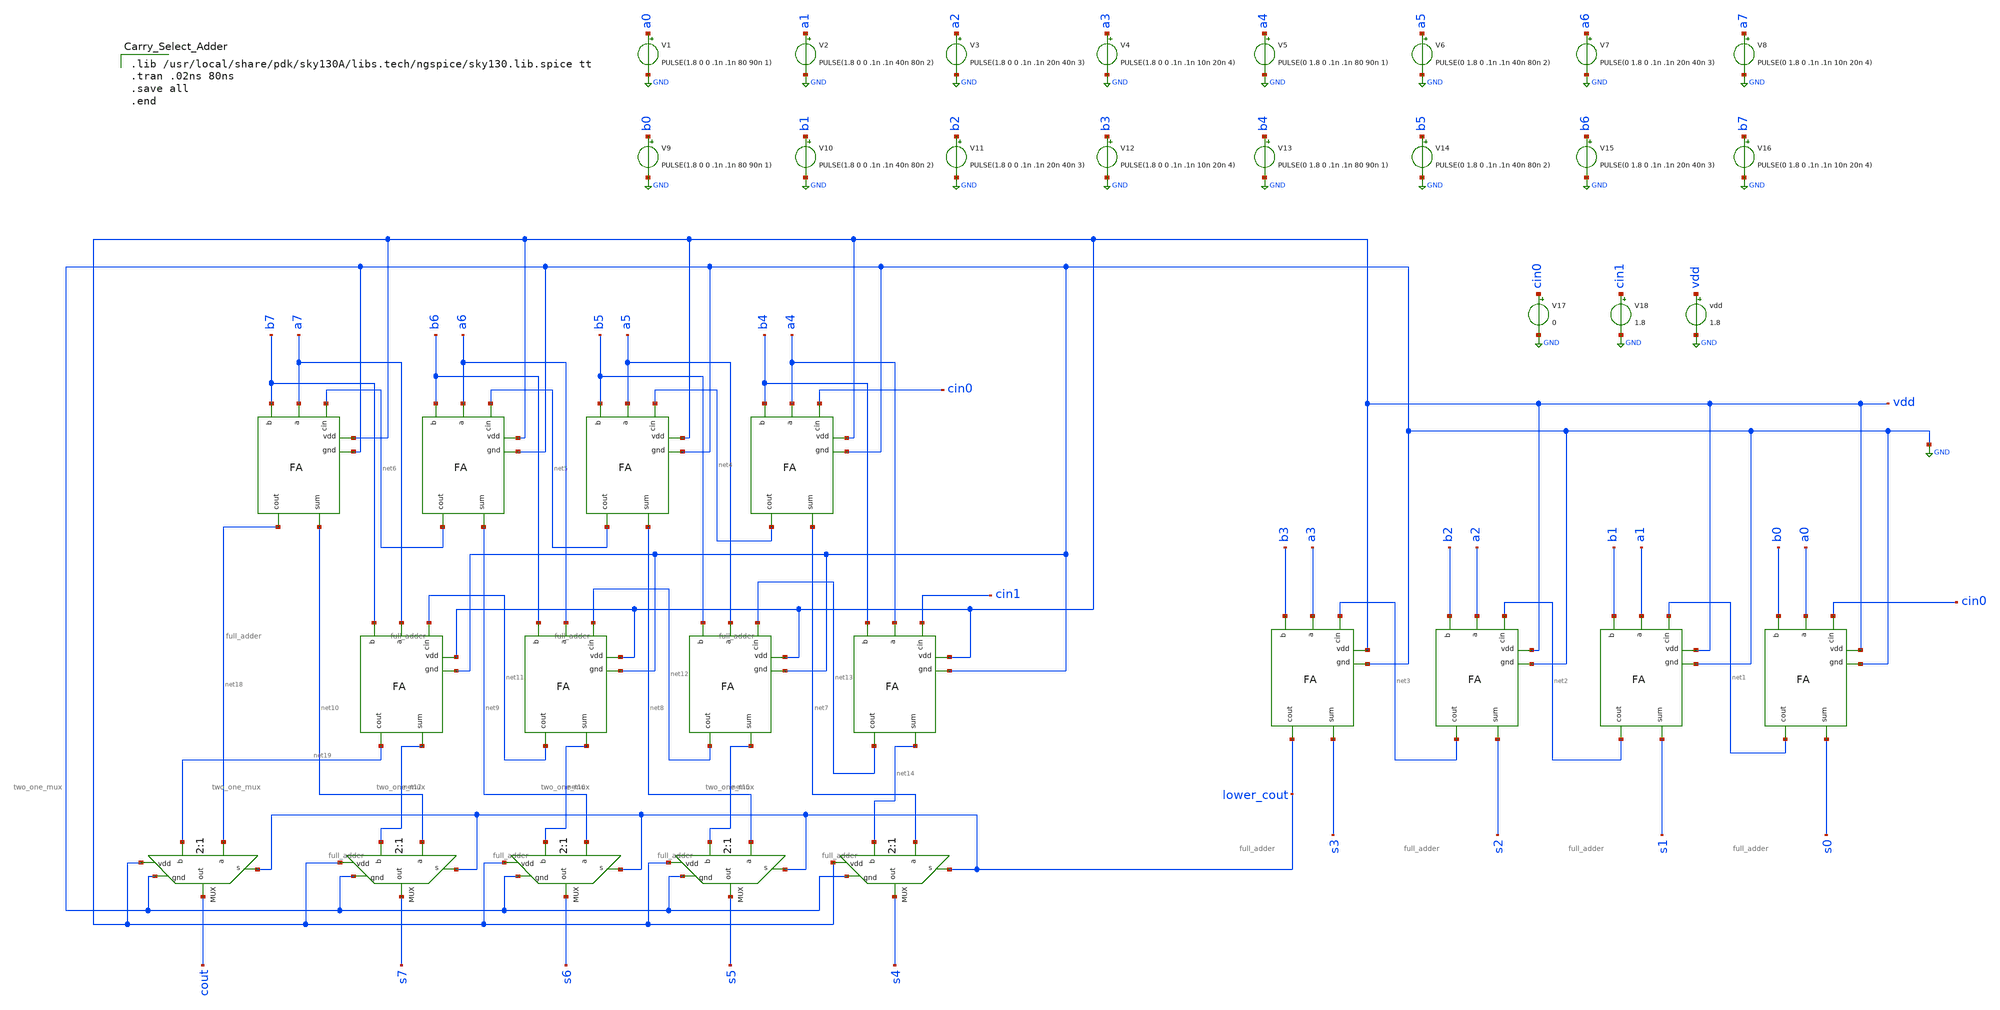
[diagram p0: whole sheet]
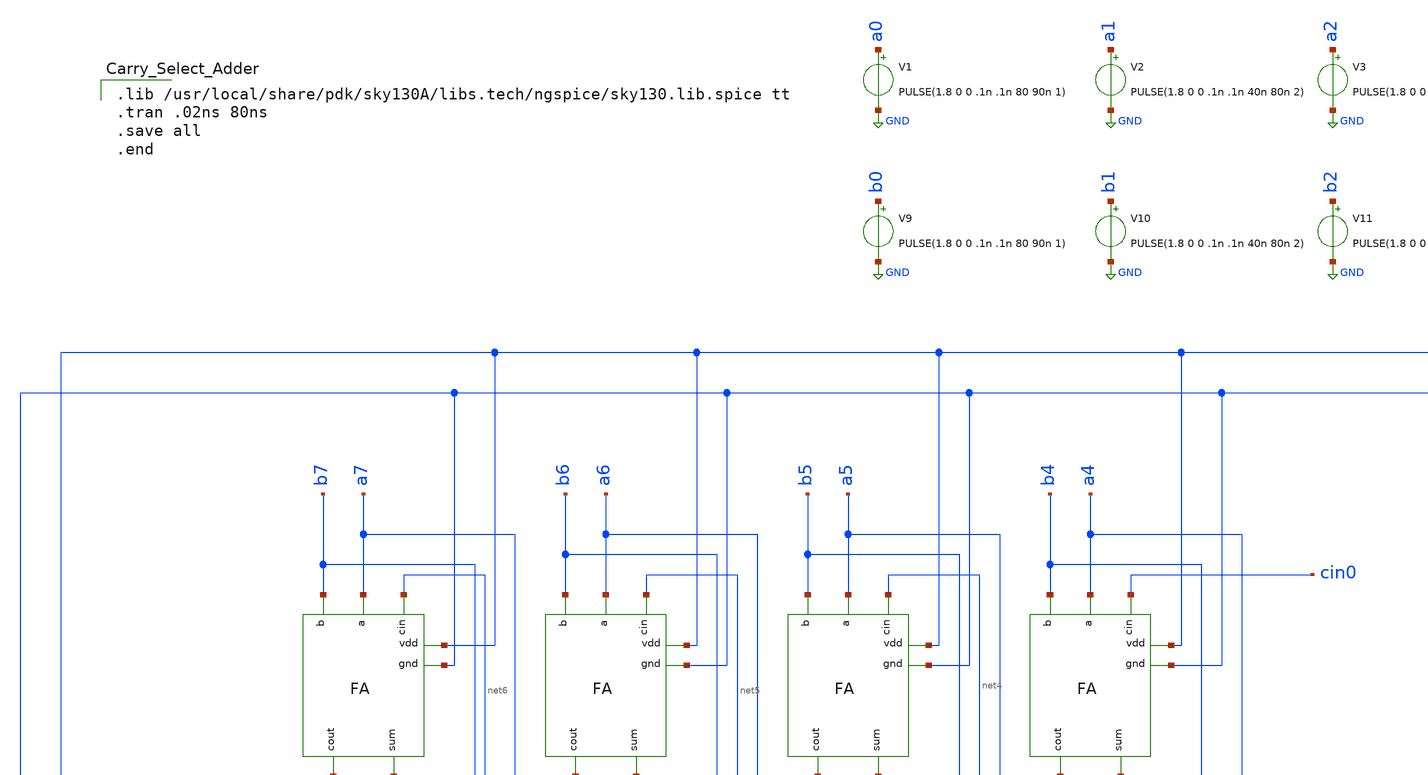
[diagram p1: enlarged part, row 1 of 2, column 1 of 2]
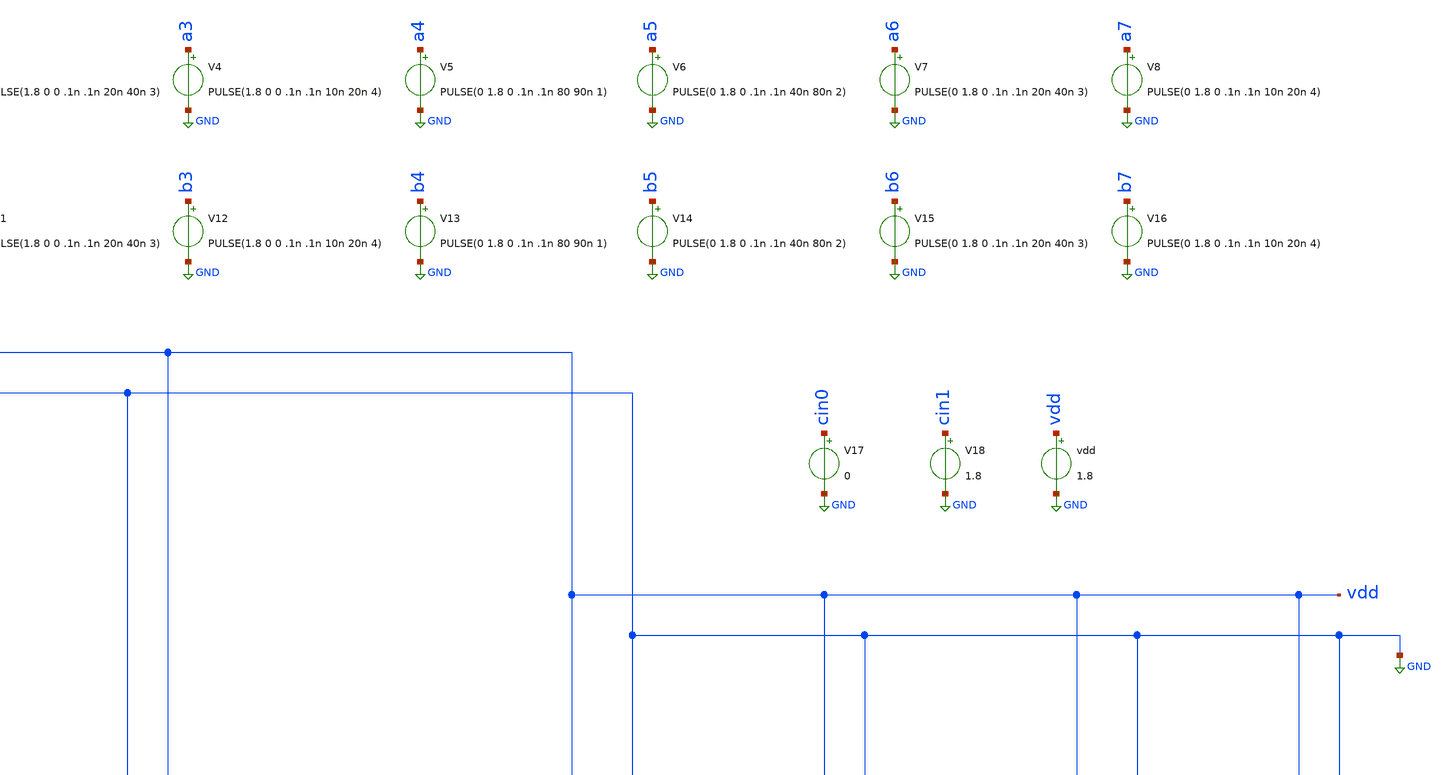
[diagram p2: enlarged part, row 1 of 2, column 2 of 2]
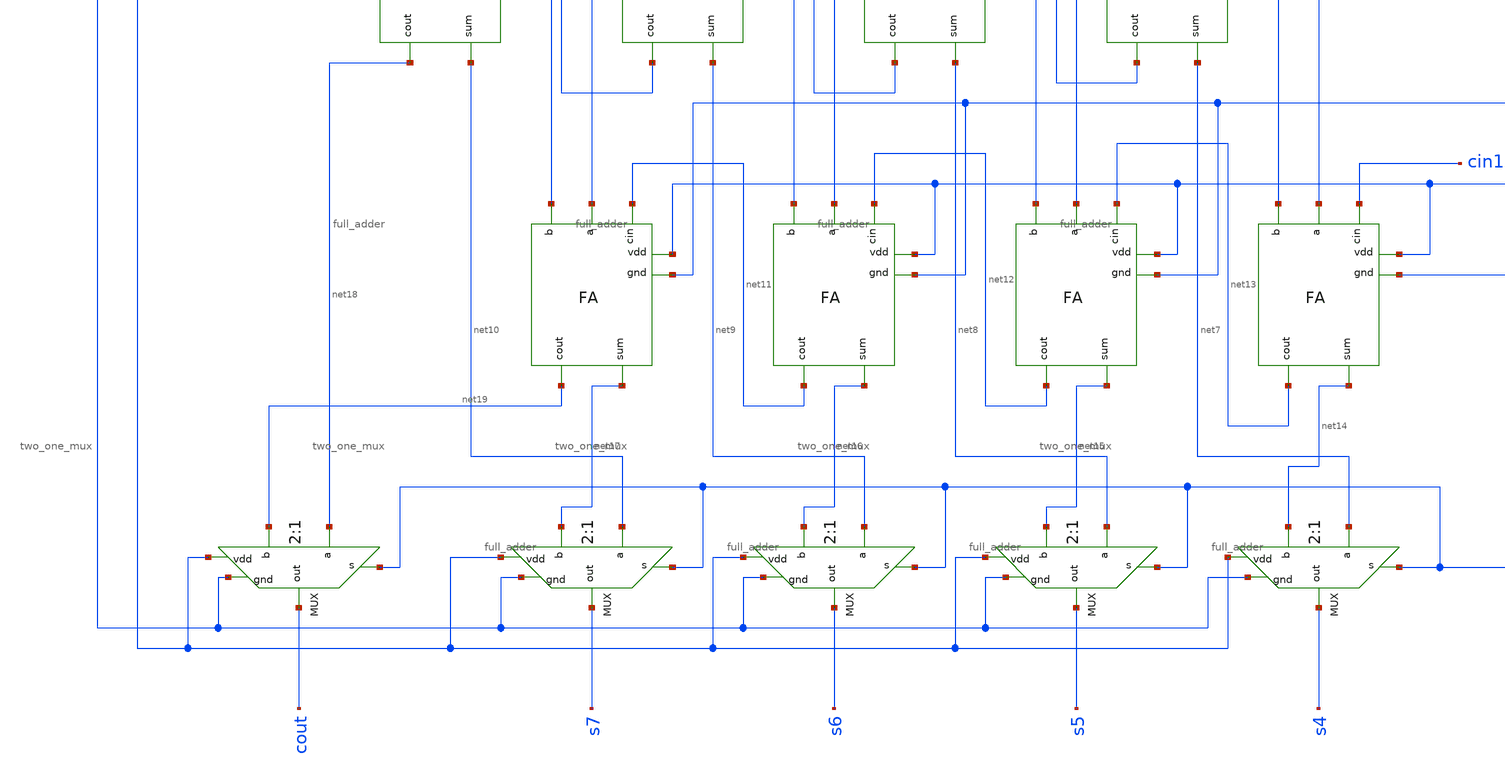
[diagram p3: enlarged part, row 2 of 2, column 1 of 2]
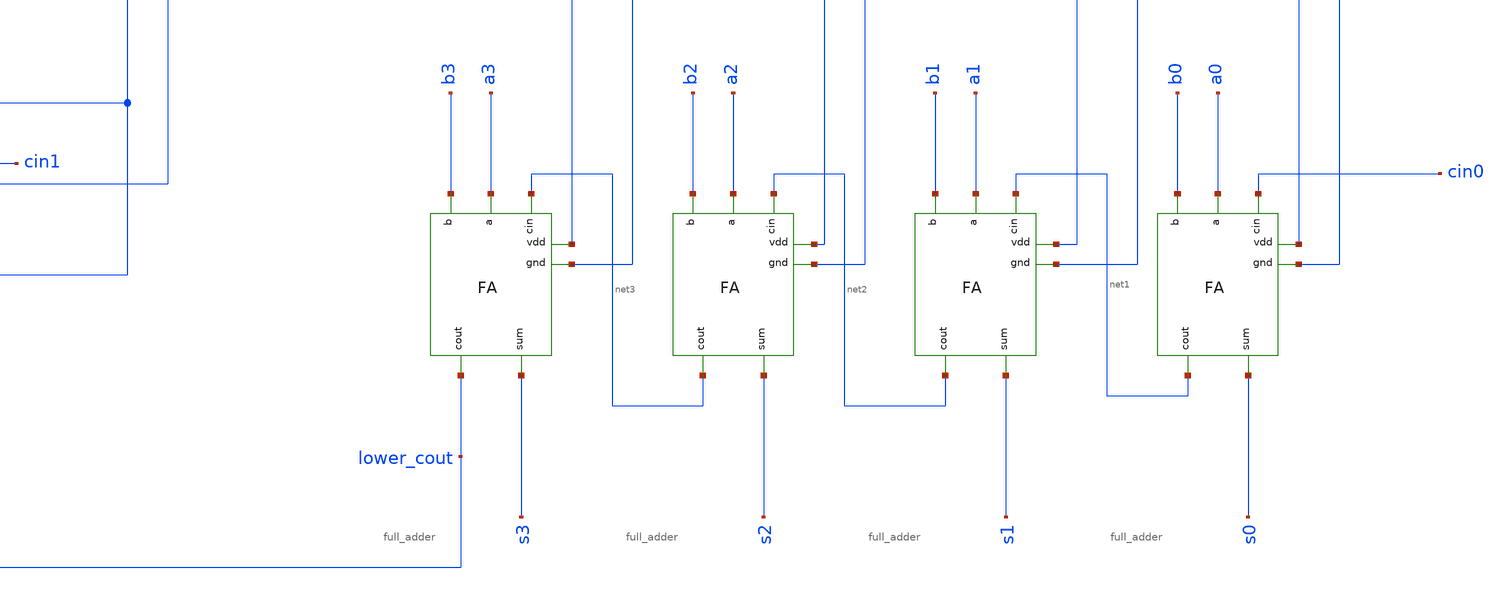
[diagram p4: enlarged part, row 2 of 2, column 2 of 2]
** sch_path: Projects/Design_and_Analysis_of_8-bit_Carry_Select_Adder_Schematic_Design_Layout_Design_and_LVS_Validation_using_SKY130PDK/assets/files/schematic/carry_select_adder.sch
**.subckt carry_select_adder
x1 s3 lower_cout vdd GND net3 a3 b3 full_adder
x2 s2 net3 vdd GND net2 a2 b2 full_adder
x3 s1 net2 vdd GND net1 a1 b1 full_adder
x4 s0 net1 vdd GND cin0 a0 b0 full_adder
x5 net10 net18 vdd GND net6 a7 b7 full_adder
x6 net9 net6 vdd GND net5 a6 b6 full_adder
x7 net8 net5 vdd GND net4 a5 b5 full_adder
x8 net7 net4 vdd GND cin0 a4 b4 full_adder
x9 net17 net19 vdd GND net11 a7 b7 full_adder
x10 net16 net11 vdd GND net12 a6 b6 full_adder
x11 net15 net12 vdd GND net13 a5 b5 full_adder
x12 net14 net13 vdd GND cin1 a4 b4 full_adder
x13 s7 lower_cout net10 net17 vdd GND two_one_mux
x14 s6 lower_cout net9 net16 vdd GND two_one_mux
x15 s5 lower_cout net8 net15 vdd GND two_one_mux
x16 s4 lower_cout net7 net14 vdd GND two_one_mux
x17 cout lower_cout net18 net19 vdd GND two_one_mux
V17 cin0 GND 0
V18 cin1 GND 1.8
vdd vdd GND 1.8
V1 a0 GND PULSE(1.8 0 0 .1n .1n 80 90n 1)
V2 a1 GND PULSE(1.8 0 0 .1n .1n 40n 80n 2)
V3 a2 GND PULSE(1.8 0 0 .1n .1n 20n 40n 3)
V4 a3 GND PULSE(1.8 0 0 .1n .1n 10n 20n 4)
V5 a4 GND PULSE(0 1.8 0 .1n .1n 80 90n 1)
V6 a5 GND PULSE(0 1.8 0 .1n .1n 40n 80n 2)
V7 a6 GND PULSE(0 1.8 0 .1n .1n 20n 40n 3)
V8 a7 GND PULSE(0 1.8 0 .1n .1n 10n 20n 4)
V9 b0 GND PULSE(1.8 0 0 .1n .1n 80 90n 1)
V10 b1 GND PULSE(1.8 0 0 .1n .1n 40n 80n 2)
V11 b2 GND PULSE(1.8 0 0 .1n .1n 20n 40n 3)
V12 b3 GND PULSE(1.8 0 0 .1n .1n 10n 20n 4)
V13 b4 GND PULSE(0 1.8 0 .1n .1n 80 90n 1)
V14 b5 GND PULSE(0 1.8 0 .1n .1n 40n 80n 2)
V15 b6 GND PULSE(0 1.8 0 .1n .1n 20n 40n 3)
V16 b7 GND PULSE(0 1.8 0 .1n .1n 10n 20n 4)
**** begin user architecture code

.lib /usr/local/share/pdk/sky130A/libs.tech/ngspice/sky130.lib.spice tt
.tran .02ns 80ns
.save all
.end

**** end user architecture code
**.ends

* expanding   symbol:  full_adder.sym # of pins=7
** sym_path: Projects/Design_and_Analysis_of_8-bit_Carry_Select_Adder_Schematic_Design_Layout_Design_and_LVS_Validation_using_SKY130PDK/assets/files/schematic/full_adder.sym
** sch_path: Projects/Design_and_Analysis_of_8-bit_Carry_Select_Adder_Schematic_Design_Layout_Design_and_LVS_Validation_using_SKY130PDK/assets/files/schematic/full_adder.sch
.subckt full_adder sum cout vdd gnd cin a b
*.ipin a
*.ipin b
*.ipin cin
*.opin cout
*.opin sum
*.ipin vdd
*.ipin gnd
XM27 sum net1 vdd vdd sky130_fd_pr__pfet_01v8 L=0.15 W=2 nf=1 ad='int((nf+1)/2) * W/nf * 0.29' as='int((nf+2)/2) * W/nf * 0.29'
+ pd='2*int((nf+1)/2) * (W/nf + 0.29)' ps='2*int((nf+2)/2) * (W/nf + 0.29)' nrd='0.29 / W' nrs='0.29 / W'
+ sa=0 sb=0 sd=0 mult=1 m=1
XM28 sum net1 gnd gnd sky130_fd_pr__nfet_01v8 L=0.15 W=1 nf=1 ad='int((nf+1)/2) * W/nf * 0.29' as='int((nf+2)/2) * W/nf * 0.29'
+ pd='2*int((nf+1)/2) * (W/nf + 0.29)' ps='2*int((nf+2)/2) * (W/nf + 0.29)' nrd='0.29 / W' nrs='0.29 / W'
+ sa=0 sb=0 sd=0 mult=1 m=1
XM11 cout net2 vdd vdd sky130_fd_pr__pfet_01v8 L=0.15 W=2 nf=1 ad='int((nf+1)/2) * W/nf * 0.29' as='int((nf+2)/2) * W/nf * 0.29'
+ pd='2*int((nf+1)/2) * (W/nf + 0.29)' ps='2*int((nf+2)/2) * (W/nf + 0.29)' nrd='0.29 / W' nrs='0.29 / W'
+ sa=0 sb=0 sd=0 mult=1 m=1
XM12 cout net2 gnd gnd sky130_fd_pr__nfet_01v8 L=0.15 W=1 nf=1 ad='int((nf+1)/2) * W/nf * 0.29' as='int((nf+2)/2) * W/nf * 0.29'
+ pd='2*int((nf+1)/2) * (W/nf + 0.29)' ps='2*int((nf+2)/2) * (W/nf + 0.29)' nrd='0.29 / W' nrs='0.29 / W'
+ sa=0 sb=0 sd=0 mult=1 m=1
XM1 net2 cin net4 gnd sky130_fd_pr__nfet_01v8 L=0.15 W=2 nf=1 ad='int((nf+1)/2) * W/nf * 0.29' as='int((nf+2)/2) * W/nf * 0.29'
+ pd='2*int((nf+1)/2) * (W/nf + 0.29)' ps='2*int((nf+2)/2) * (W/nf + 0.29)' nrd='0.29 / W' nrs='0.29 / W'
+ sa=0 sb=0 sd=0 mult=1 m=1
XM2 net3 a vdd vdd sky130_fd_pr__pfet_01v8 L=0.15 W=4 nf=1 ad='int((nf+1)/2) * W/nf * 0.29' as='int((nf+2)/2) * W/nf * 0.29'
+ pd='2*int((nf+1)/2) * (W/nf + 0.29)' ps='2*int((nf+2)/2) * (W/nf + 0.29)' nrd='0.29 / W' nrs='0.29 / W'
+ sa=0 sb=0 sd=0 mult=1 m=1
XM3 net3 b vdd vdd sky130_fd_pr__pfet_01v8 L=0.15 W=4 nf=1 ad='int((nf+1)/2) * W/nf * 0.29' as='int((nf+2)/2) * W/nf * 0.29'
+ pd='2*int((nf+1)/2) * (W/nf + 0.29)' ps='2*int((nf+2)/2) * (W/nf + 0.29)' nrd='0.29 / W' nrs='0.29 / W'
+ sa=0 sb=0 sd=0 mult=1 m=1
XM4 net2 cin net3 vdd sky130_fd_pr__pfet_01v8 L=0.15 W=4 nf=1 ad='int((nf+1)/2) * W/nf * 0.29' as='int((nf+2)/2) * W/nf * 0.29'
+ pd='2*int((nf+1)/2) * (W/nf + 0.29)' ps='2*int((nf+2)/2) * (W/nf + 0.29)' nrd='0.29 / W' nrs='0.29 / W'
+ sa=0 sb=0 sd=0 mult=1 m=1
XM5 net4 a gnd gnd sky130_fd_pr__nfet_01v8 L=0.15 W=2 nf=1 ad='int((nf+1)/2) * W/nf * 0.29' as='int((nf+2)/2) * W/nf * 0.29'
+ pd='2*int((nf+1)/2) * (W/nf + 0.29)' ps='2*int((nf+2)/2) * (W/nf + 0.29)' nrd='0.29 / W' nrs='0.29 / W'
+ sa=0 sb=0 sd=0 mult=1 m=1
XM6 net4 b gnd gnd sky130_fd_pr__nfet_01v8 L=0.15 W=2 nf=1 ad='int((nf+1)/2) * W/nf * 0.29' as='int((nf+2)/2) * W/nf * 0.29'
+ pd='2*int((nf+1)/2) * (W/nf + 0.29)' ps='2*int((nf+2)/2) * (W/nf + 0.29)' nrd='0.29 / W' nrs='0.29 / W'
+ sa=0 sb=0 sd=0 mult=1 m=1
XM7 net2 a net6 vdd sky130_fd_pr__pfet_01v8 L=0.15 W=4 nf=1 ad='int((nf+1)/2) * W/nf * 0.29' as='int((nf+2)/2) * W/nf * 0.29'
+ pd='2*int((nf+1)/2) * (W/nf + 0.29)' ps='2*int((nf+2)/2) * (W/nf + 0.29)' nrd='0.29 / W' nrs='0.29 / W'
+ sa=0 sb=0 sd=0 mult=1 m=1
XM8 net6 b vdd vdd sky130_fd_pr__pfet_01v8 L=0.15 W=4 nf=1 ad='int((nf+1)/2) * W/nf * 0.29' as='int((nf+2)/2) * W/nf * 0.29'
+ pd='2*int((nf+1)/2) * (W/nf + 0.29)' ps='2*int((nf+2)/2) * (W/nf + 0.29)' nrd='0.29 / W' nrs='0.29 / W'
+ sa=0 sb=0 sd=0 mult=1 m=1
XM9 net2 a net5 gnd sky130_fd_pr__nfet_01v8 L=0.15 W=2 nf=1 ad='int((nf+1)/2) * W/nf * 0.29' as='int((nf+2)/2) * W/nf * 0.29'
+ pd='2*int((nf+1)/2) * (W/nf + 0.29)' ps='2*int((nf+2)/2) * (W/nf + 0.29)' nrd='0.29 / W' nrs='0.29 / W'
+ sa=0 sb=0 sd=0 mult=1 m=1
XM10 net5 b gnd gnd sky130_fd_pr__nfet_01v8 L=0.15 W=2 nf=1 ad='int((nf+1)/2) * W/nf * 0.29' as='int((nf+2)/2) * W/nf * 0.29'
+ pd='2*int((nf+1)/2) * (W/nf + 0.29)' ps='2*int((nf+2)/2) * (W/nf + 0.29)' nrd='0.29 / W' nrs='0.29 / W'
+ sa=0 sb=0 sd=0 mult=1 m=1
XM13 net8 a vdd vdd sky130_fd_pr__pfet_01v8 L=0.15 W=4 nf=1 ad='int((nf+1)/2) * W/nf * 0.29' as='int((nf+2)/2) * W/nf * 0.29'
+ pd='2*int((nf+1)/2) * (W/nf + 0.29)' ps='2*int((nf+2)/2) * (W/nf + 0.29)' nrd='0.29 / W' nrs='0.29 / W'
+ sa=0 sb=0 sd=0 mult=1 m=1
XM14 net8 b vdd vdd sky130_fd_pr__pfet_01v8 L=0.15 W=4 nf=1 ad='int((nf+1)/2) * W/nf * 0.29' as='int((nf+2)/2) * W/nf * 0.29'
+ pd='2*int((nf+1)/2) * (W/nf + 0.29)' ps='2*int((nf+2)/2) * (W/nf + 0.29)' nrd='0.29 / W' nrs='0.29 / W'
+ sa=0 sb=0 sd=0 mult=1 m=1
XM15 net8 cin vdd vdd sky130_fd_pr__pfet_01v8 L=0.15 W=4 nf=1 ad='int((nf+1)/2) * W/nf * 0.29' as='int((nf+2)/2) * W/nf * 0.29'
+ pd='2*int((nf+1)/2) * (W/nf + 0.29)' ps='2*int((nf+2)/2) * (W/nf + 0.29)' nrd='0.29 / W' nrs='0.29 / W'
+ sa=0 sb=0 sd=0 mult=1 m=1
XM16 net7 a gnd gnd sky130_fd_pr__nfet_01v8 L=0.15 W=2 nf=1 ad='int((nf+1)/2) * W/nf * 0.29' as='int((nf+2)/2) * W/nf * 0.29'
+ pd='2*int((nf+1)/2) * (W/nf + 0.29)' ps='2*int((nf+2)/2) * (W/nf + 0.29)' nrd='0.29 / W' nrs='0.29 / W'
+ sa=0 sb=0 sd=0 mult=1 m=1
XM17 net7 b gnd gnd sky130_fd_pr__nfet_01v8 L=0.15 W=2 nf=1 ad='int((nf+1)/2) * W/nf * 0.29' as='int((nf+2)/2) * W/nf * 0.29'
+ pd='2*int((nf+1)/2) * (W/nf + 0.29)' ps='2*int((nf+2)/2) * (W/nf + 0.29)' nrd='0.29 / W' nrs='0.29 / W'
+ sa=0 sb=0 sd=0 mult=1 m=1
XM18 net7 cin gnd gnd sky130_fd_pr__nfet_01v8 L=0.15 W=2 nf=1 ad='int((nf+1)/2) * W/nf * 0.29' as='int((nf+2)/2) * W/nf * 0.29'
+ pd='2*int((nf+1)/2) * (W/nf + 0.29)' ps='2*int((nf+2)/2) * (W/nf + 0.29)' nrd='0.29 / W' nrs='0.29 / W'
+ sa=0 sb=0 sd=0 mult=1 m=1
XM19 net1 net2 net7 gnd sky130_fd_pr__nfet_01v8 L=0.15 W=2 nf=1 ad='int((nf+1)/2) * W/nf * 0.29' as='int((nf+2)/2) * W/nf * 0.29'
+ pd='2*int((nf+1)/2) * (W/nf + 0.29)' ps='2*int((nf+2)/2) * (W/nf + 0.29)' nrd='0.29 / W' nrs='0.29 / W'
+ sa=0 sb=0 sd=0 mult=1 m=1
XM20 net1 net2 net8 vdd sky130_fd_pr__pfet_01v8 L=0.15 W=4 nf=1 ad='int((nf+1)/2) * W/nf * 0.29' as='int((nf+2)/2) * W/nf * 0.29'
+ pd='2*int((nf+1)/2) * (W/nf + 0.29)' ps='2*int((nf+2)/2) * (W/nf + 0.29)' nrd='0.29 / W' nrs='0.29 / W'
+ sa=0 sb=0 sd=0 mult=1 m=1
XM21 net1 cin net10 vdd sky130_fd_pr__pfet_01v8 L=0.15 W=6 nf=1 ad='int((nf+1)/2) * W/nf * 0.29' as='int((nf+2)/2) * W/nf * 0.29'
+ pd='2*int((nf+1)/2) * (W/nf + 0.29)' ps='2*int((nf+2)/2) * (W/nf + 0.29)' nrd='0.29 / W' nrs='0.29 / W'
+ sa=0 sb=0 sd=0 mult=1 m=1
XM22 net10 b net9 vdd sky130_fd_pr__pfet_01v8 L=0.15 W=6 nf=1 ad='int((nf+1)/2) * W/nf * 0.29' as='int((nf+2)/2) * W/nf * 0.29'
+ pd='2*int((nf+1)/2) * (W/nf + 0.29)' ps='2*int((nf+2)/2) * (W/nf + 0.29)' nrd='0.29 / W' nrs='0.29 / W'
+ sa=0 sb=0 sd=0 mult=1 m=1
XM23 net9 a vdd vdd sky130_fd_pr__pfet_01v8 L=0.15 W=6 nf=1 ad='int((nf+1)/2) * W/nf * 0.29' as='int((nf+2)/2) * W/nf * 0.29'
+ pd='2*int((nf+1)/2) * (W/nf + 0.29)' ps='2*int((nf+2)/2) * (W/nf + 0.29)' nrd='0.29 / W' nrs='0.29 / W'
+ sa=0 sb=0 sd=0 mult=1 m=1
XM24 net1 cin net12 gnd sky130_fd_pr__nfet_01v8 L=0.15 W=3 nf=1 ad='int((nf+1)/2) * W/nf * 0.29' as='int((nf+2)/2) * W/nf * 0.29'
+ pd='2*int((nf+1)/2) * (W/nf + 0.29)' ps='2*int((nf+2)/2) * (W/nf + 0.29)' nrd='0.29 / W' nrs='0.29 / W'
+ sa=0 sb=0 sd=0 mult=1 m=1
XM25 net12 b net11 gnd sky130_fd_pr__nfet_01v8 L=0.15 W=3 nf=1 ad='int((nf+1)/2) * W/nf * 0.29' as='int((nf+2)/2) * W/nf * 0.29'
+ pd='2*int((nf+1)/2) * (W/nf + 0.29)' ps='2*int((nf+2)/2) * (W/nf + 0.29)' nrd='0.29 / W' nrs='0.29 / W'
+ sa=0 sb=0 sd=0 mult=1 m=1
XM26 net11 a gnd gnd sky130_fd_pr__nfet_01v8 L=0.15 W=3 nf=1 ad='int((nf+1)/2) * W/nf * 0.29' as='int((nf+2)/2) * W/nf * 0.29'
+ pd='2*int((nf+1)/2) * (W/nf + 0.29)' ps='2*int((nf+2)/2) * (W/nf + 0.29)' nrd='0.29 / W' nrs='0.29 / W'
+ sa=0 sb=0 sd=0 mult=1 m=1
.ends


* expanding   symbol:  two_one_mux.sym # of pins=6
** sym_path: Projects/testfolder/two_one_mux.sym
** sch_path: Projects/testfolder/two_one_mux.sch
.subckt two_one_mux out s a b vdd gnd
*.ipin a
*.ipin b
*.ipin s
*.ipin vdd
*.ipin gnd
*.opin out
XM1 net1 s vdd vdd sky130_fd_pr__pfet_01v8 L=0.15 W=2 nf=1 ad='int((nf+1)/2) * W/nf * 0.29' as='int((nf+2)/2) * W/nf * 0.29'
+ pd='2*int((nf+1)/2) * (W/nf + 0.29)' ps='2*int((nf+2)/2) * (W/nf + 0.29)' nrd='0.29 / W' nrs='0.29 / W'
+ sa=0 sb=0 sd=0 mult=1 m=1
XM4 net1 s gnd gnd sky130_fd_pr__nfet_01v8 L=0.15 W=1 nf=1 ad='int((nf+1)/2) * W/nf * 0.29' as='int((nf+2)/2) * W/nf * 0.29'
+ pd='2*int((nf+1)/2) * (W/nf + 0.29)' ps='2*int((nf+2)/2) * (W/nf + 0.29)' nrd='0.29 / W' nrs='0.29 / W'
+ sa=0 sb=0 sd=0 mult=1 m=1
XM2 net4 net1 net2 gnd sky130_fd_pr__nfet_01v8 L=0.15 W=2 nf=1 ad='int((nf+1)/2) * W/nf * 0.29' as='int((nf+2)/2) * W/nf * 0.29'
+ pd='2*int((nf+1)/2) * (W/nf + 0.29)' ps='2*int((nf+2)/2) * (W/nf + 0.29)' nrd='0.29 / W' nrs='0.29 / W'
+ sa=0 sb=0 sd=0 mult=1 m=1
XM3 net2 a gnd gnd sky130_fd_pr__nfet_01v8 L=0.15 W=2 nf=1 ad='int((nf+1)/2) * W/nf * 0.29' as='int((nf+2)/2) * W/nf * 0.29'
+ pd='2*int((nf+1)/2) * (W/nf + 0.29)' ps='2*int((nf+2)/2) * (W/nf + 0.29)' nrd='0.29 / W' nrs='0.29 / W'
+ sa=0 sb=0 sd=0 mult=1 m=1
XM5 net4 s net3 gnd sky130_fd_pr__nfet_01v8 L=0.15 W=2 nf=1 ad='int((nf+1)/2) * W/nf * 0.29' as='int((nf+2)/2) * W/nf * 0.29'
+ pd='2*int((nf+1)/2) * (W/nf + 0.29)' ps='2*int((nf+2)/2) * (W/nf + 0.29)' nrd='0.29 / W' nrs='0.29 / W'
+ sa=0 sb=0 sd=0 mult=1 m=1
XM6 net3 b gnd gnd sky130_fd_pr__nfet_01v8 L=0.15 W=2 nf=1 ad='int((nf+1)/2) * W/nf * 0.29' as='int((nf+2)/2) * W/nf * 0.29'
+ pd='2*int((nf+1)/2) * (W/nf + 0.29)' ps='2*int((nf+2)/2) * (W/nf + 0.29)' nrd='0.29 / W' nrs='0.29 / W'
+ sa=0 sb=0 sd=0 mult=1 m=1
XM7 net4 net1 net5 vdd sky130_fd_pr__pfet_01v8 L=0.15 W=4 nf=1 ad='int((nf+1)/2) * W/nf * 0.29' as='int((nf+2)/2) * W/nf * 0.29'
+ pd='2*int((nf+1)/2) * (W/nf + 0.29)' ps='2*int((nf+2)/2) * (W/nf + 0.29)' nrd='0.29 / W' nrs='0.29 / W'
+ sa=0 sb=0 sd=0 mult=1 m=1
XM8 net5 s vdd vdd sky130_fd_pr__pfet_01v8 L=0.15 W=4 nf=1 ad='int((nf+1)/2) * W/nf * 0.29' as='int((nf+2)/2) * W/nf * 0.29'
+ pd='2*int((nf+1)/2) * (W/nf + 0.29)' ps='2*int((nf+2)/2) * (W/nf + 0.29)' nrd='0.29 / W' nrs='0.29 / W'
+ sa=0 sb=0 sd=0 mult=1 m=1
XM9 net4 a net5 vdd sky130_fd_pr__pfet_01v8 L=0.15 W=4 nf=1 ad='int((nf+1)/2) * W/nf * 0.29' as='int((nf+2)/2) * W/nf * 0.29'
+ pd='2*int((nf+1)/2) * (W/nf + 0.29)' ps='2*int((nf+2)/2) * (W/nf + 0.29)' nrd='0.29 / W' nrs='0.29 / W'
+ sa=0 sb=0 sd=0 mult=1 m=1
XM10 net5 b vdd vdd sky130_fd_pr__pfet_01v8 L=0.15 W=4 nf=1 ad='int((nf+1)/2) * W/nf * 0.29' as='int((nf+2)/2) * W/nf * 0.29'
+ pd='2*int((nf+1)/2) * (W/nf + 0.29)' ps='2*int((nf+2)/2) * (W/nf + 0.29)' nrd='0.29 / W' nrs='0.29 / W'
+ sa=0 sb=0 sd=0 mult=1 m=1
XM11 out net4 vdd vdd sky130_fd_pr__pfet_01v8 L=0.15 W=2 nf=1 ad='int((nf+1)/2) * W/nf * 0.29' as='int((nf+2)/2) * W/nf * 0.29'
+ pd='2*int((nf+1)/2) * (W/nf + 0.29)' ps='2*int((nf+2)/2) * (W/nf + 0.29)' nrd='0.29 / W' nrs='0.29 / W'
+ sa=0 sb=0 sd=0 mult=1 m=1
XM12 out net4 gnd gnd sky130_fd_pr__nfet_01v8 L=0.15 W=1 nf=1 ad='int((nf+1)/2) * W/nf * 0.29' as='int((nf+2)/2) * W/nf * 0.29'
+ pd='2*int((nf+1)/2) * (W/nf + 0.29)' ps='2*int((nf+2)/2) * (W/nf + 0.29)' nrd='0.29 / W' nrs='0.29 / W'
+ sa=0 sb=0 sd=0 mult=1 m=1
.ends

.GLOBAL GND
.end
